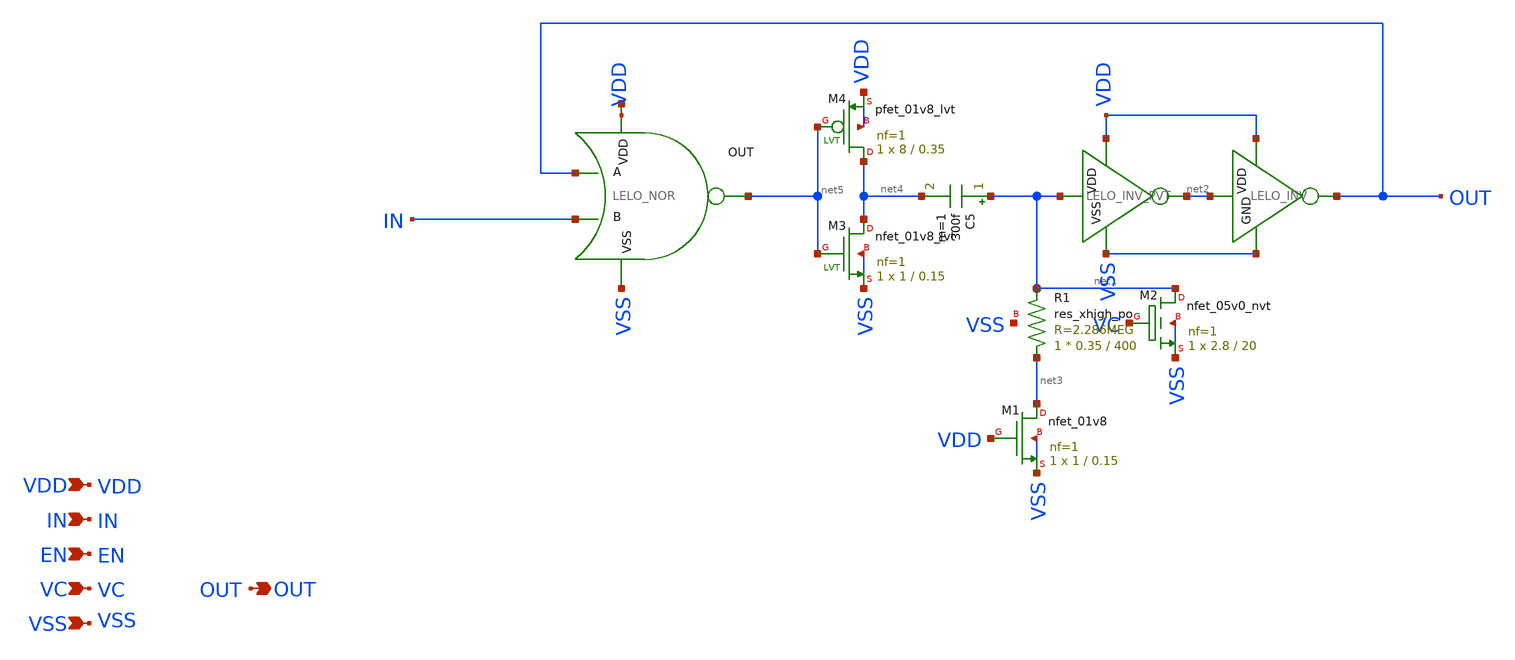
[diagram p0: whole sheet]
** sch_path: design/LELO_SVOD_SKY130A/LELO_ONESHOT_VC2.sch
**.subckt LELO_ONESHOT_VC2 VDD IN VC VSS OUT EN
*.ipin VDD
*.ipin IN
*.ipin VC
*.ipin VSS
*.opin OUT
*.ipin EN
x2 net6 net5 OUT IN VSS LELO_NOR
C5 net1 net4 300f m=1
x4 VDD net2 OUT VSS LELO_INV
XM2 net1 VC VSS VSS sky130_fd_pr__nfet_05v0_nvt L=20 W=2.8 nf=1 ad='int((1 + 1)/2) * 2.8 / 1 * 0.29'
+ as='int((1 + 2)/2) * 2.8 / 1 * 0.29' pd='2*int((1 + 1)/2) * (2.8 / 1 + 0.29)' ps='2*int((1 + 2)/2) * (2.8 / 1 + 0.29)'
+ nrd='0.29 / 2.8 ' nrs='0.29 / 2.8 ' sa=0 sb=0 sd=0 mult=1 m=1
XR1 net3 net1 VSS sky130_fd_pr__res_xhigh_po W=0.35 L=400 mult=1 m=1
XM1 net3 VDD VSS VSS sky130_fd_pr__nfet_01v8 L=0.15 W=1 nf=1 ad='int((1 + 1)/2) * 1 / 1 * 0.29' as='int((1 + 2)/2) * 1 / 1 * 0.29'
+ pd='2*int((1 + 1)/2) * (1 / 1 + 0.29)' ps='2*int((1 + 2)/2) * (1 / 1 + 0.29)' nrd='0.29 / 1 ' nrs='0.29 / 1 '
+ sa=0 sb=0 sd=0 mult=1 m=1
x3 VDD net1 net2 VSS LELO_INV_PVT
XM3 net4 net5 VSS VSS sky130_fd_pr__nfet_01v8_lvt L=0.15 W=1 nf=1 ad='int((1 + 1)/2) * 1 / 1 * 0.29'
+ as='int((1 + 2)/2) * 1 / 1 * 0.29' pd='2*int((1 + 1)/2) * (1 / 1 + 0.29)' ps='2*int((1 + 2)/2) * (1 / 1 + 0.29)'
+ nrd='0.29 / 1 ' nrs='0.29 / 1 ' sa=0 sb=0 sd=0 mult=1 m=1
XM4 net4 net5 VDD VDD sky130_fd_pr__pfet_01v8_lvt L=0.35 W=8 nf=1 ad='int((1 + 1)/2) * 8 / 1 * 0.29'
+ as='int((1 + 2)/2) * 8 / 1 * 0.29' pd='2*int((1 + 1)/2) * (8 / 1 + 0.29)' ps='2*int((1 + 2)/2) * (8 / 1 + 0.29)'
+ nrd='0.29 / 8 ' nrs='0.29 / 8 ' sa=0 sb=0 sd=0 mult=1 m=1
**.ends

* expanding   symbol:  LELO_SVOD_SKY130A/LELO_NOR.sym # of pins=5
** sym_path: design/LELO_SVOD_SKY130A/LELO_NOR.sym
** sch_path: design/LELO_SVOD_SKY130A/LELO_NOR.sch
.subckt LELO_NOR VDD OUT A B VSS
*.ipin VDD
*.ipin VSS
*.opin OUT
*.ipin A
*.ipin B
XM2 OUT B VSS VSS sky130_fd_pr__nfet_01v8 L=0.15 W=2 nf=1 ad='int((1 + 1)/2) * 2 / 1 * 0.29' as='int((1 + 2)/2) * 2 / 1 * 0.29'
+ pd='2*int((1 + 1)/2) * (2 / 1 + 0.29)' ps='2*int((1 + 2)/2) * (2 / 1 + 0.29)' nrd='0.29 / 2 ' nrs='0.29 / 2 '
+ sa=0 sb=0 sd=0 mult=1 m=1
XM1 OUT A VSS VSS sky130_fd_pr__nfet_01v8 L=0.15 W=2 nf=1 ad='int((1 + 1)/2) * 2 / 1 * 0.29' as='int((1 + 2)/2) * 2 / 1 * 0.29'
+ pd='2*int((1 + 1)/2) * (2 / 1 + 0.29)' ps='2*int((1 + 2)/2) * (2 / 1 + 0.29)' nrd='0.29 / 2 ' nrs='0.29 / 2 '
+ sa=0 sb=0 sd=0 mult=1 m=1
XM3 OUT B net1 VDD sky130_fd_pr__pfet_01v8 L=0.15 W=4 nf=1 ad='int((1 + 1)/2) * 4 / 1 * 0.29' as='int((1 + 2)/2) * 4 / 1 * 0.29'
+ pd='2*int((1 + 1)/2) * (4 / 1 + 0.29)' ps='2*int((1 + 2)/2) * (4 / 1 + 0.29)' nrd='0.29 / 4 ' nrs='0.29 / 4 '
+ sa=0 sb=0 sd=0 mult=1 m=1
XM4 net1 A VDD VDD sky130_fd_pr__pfet_01v8 L=0.15 W=4 nf=1 ad='int((1 + 1)/2) * 4 / 1 * 0.29' as='int((1 + 2)/2) * 4 / 1 * 0.29'
+ pd='2*int((1 + 1)/2) * (4 / 1 + 0.29)' ps='2*int((1 + 2)/2) * (4 / 1 + 0.29)' nrd='0.29 / 4 ' nrs='0.29 / 4 '
+ sa=0 sb=0 sd=0 mult=1 m=1
.ends


* expanding   symbol:  LELO_SVOD_SKY130A/LELO_INV.sym # of pins=4
** sym_path: design/LELO_SVOD_SKY130A/LELO_INV.sym
** sch_path: design/LELO_SVOD_SKY130A/LELO_INV.sch
.subckt LELO_INV VDD VIN VOUT GND
*.ipin VIN
*.ipin VDD
*.ipin GND
*.opin VOUT
XM1 VOUT VIN GND GND sky130_fd_pr__nfet_01v8_lvt L=0.15 W=1 nf=1 ad='int((1 + 1)/2) * 1 / 1 * 0.29' as='int((1 + 2)/2) * 1 / 1 * 0.29'
+ pd='2*int((1 + 1)/2) * (1 / 1 + 0.29)' ps='2*int((1 + 2)/2) * (1 / 1 + 0.29)' nrd='0.29 / 1 ' nrs='0.29 / 1 '
+ sa=0 sb=0 sd=0 mult=1 m=1
XM2 VOUT VIN VDD VDD sky130_fd_pr__pfet_01v8_lvt L=0.35 W=1 nf=1 ad='int((1 + 1)/2) * 1 / 1 * 0.29' as='int((1 + 2)/2) * 1 / 1 * 0.29'
+ pd='2*int((1 + 1)/2) * (1 / 1 + 0.29)' ps='2*int((1 + 2)/2) * (1 / 1 + 0.29)' nrd='0.29 / 1 ' nrs='0.29 / 1 '
+ sa=0 sb=0 sd=0 mult=2 m=2
.ends


* expanding   symbol:  LELO_SVOD_SKY130A/LELO_INV_PVT.sym # of pins=4
** sym_path: design/LELO_SVOD_SKY130A/LELO_INV_PVT.sym
** sch_path: design/LELO_SVOD_SKY130A/LELO_INV_PVT.sch
.subckt LELO_INV_PVT VDD VIN VOUT VSS
*.ipin VIN
*.ipin VDD
*.ipin VSS
*.opin VOUT
XM1 VOUT VIN VSS VSS sky130_fd_pr__nfet_01v8_lvt L=1 W=8 nf=1 ad='int((1 + 1)/2) * 8 / 1 * 0.29' as='int((1 + 2)/2) * 8 / 1 * 0.29'
+ pd='2*int((1 + 1)/2) * (8 / 1 + 0.29)' ps='2*int((1 + 2)/2) * (8 / 1 + 0.29)' nrd='0.29 / 8 ' nrs='0.29 / 8 '
+ sa=0 sb=0 sd=0 mult=1 m=1
XM2 VOUT VIN VDD VDD sky130_fd_pr__pfet_01v8 L=0.15 W=20 nf=1 ad='int((1 + 1)/2) * 20 / 1 * 0.29' as='int((1 + 2)/2) * 20 / 1 * 0.29'
+ pd='2*int((1 + 1)/2) * (20 / 1 + 0.29)' ps='2*int((1 + 2)/2) * (20 / 1 + 0.29)' nrd='0.29 / 20 ' nrs='0.29 / 20 '
+ sa=0 sb=0 sd=0 mult=1 m=1
.ends

.end
